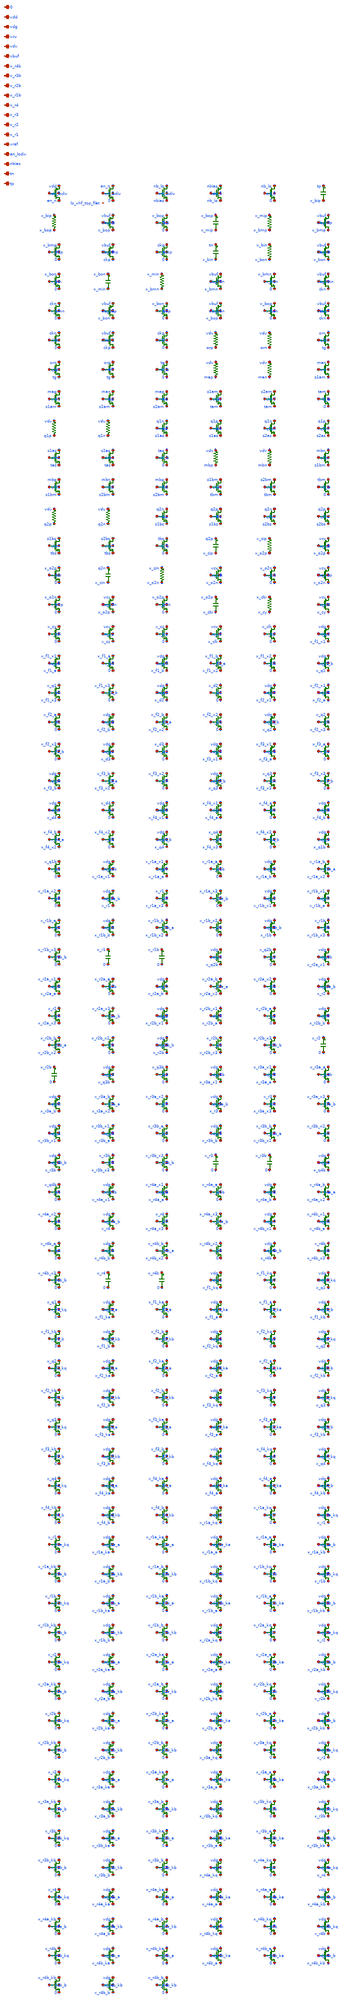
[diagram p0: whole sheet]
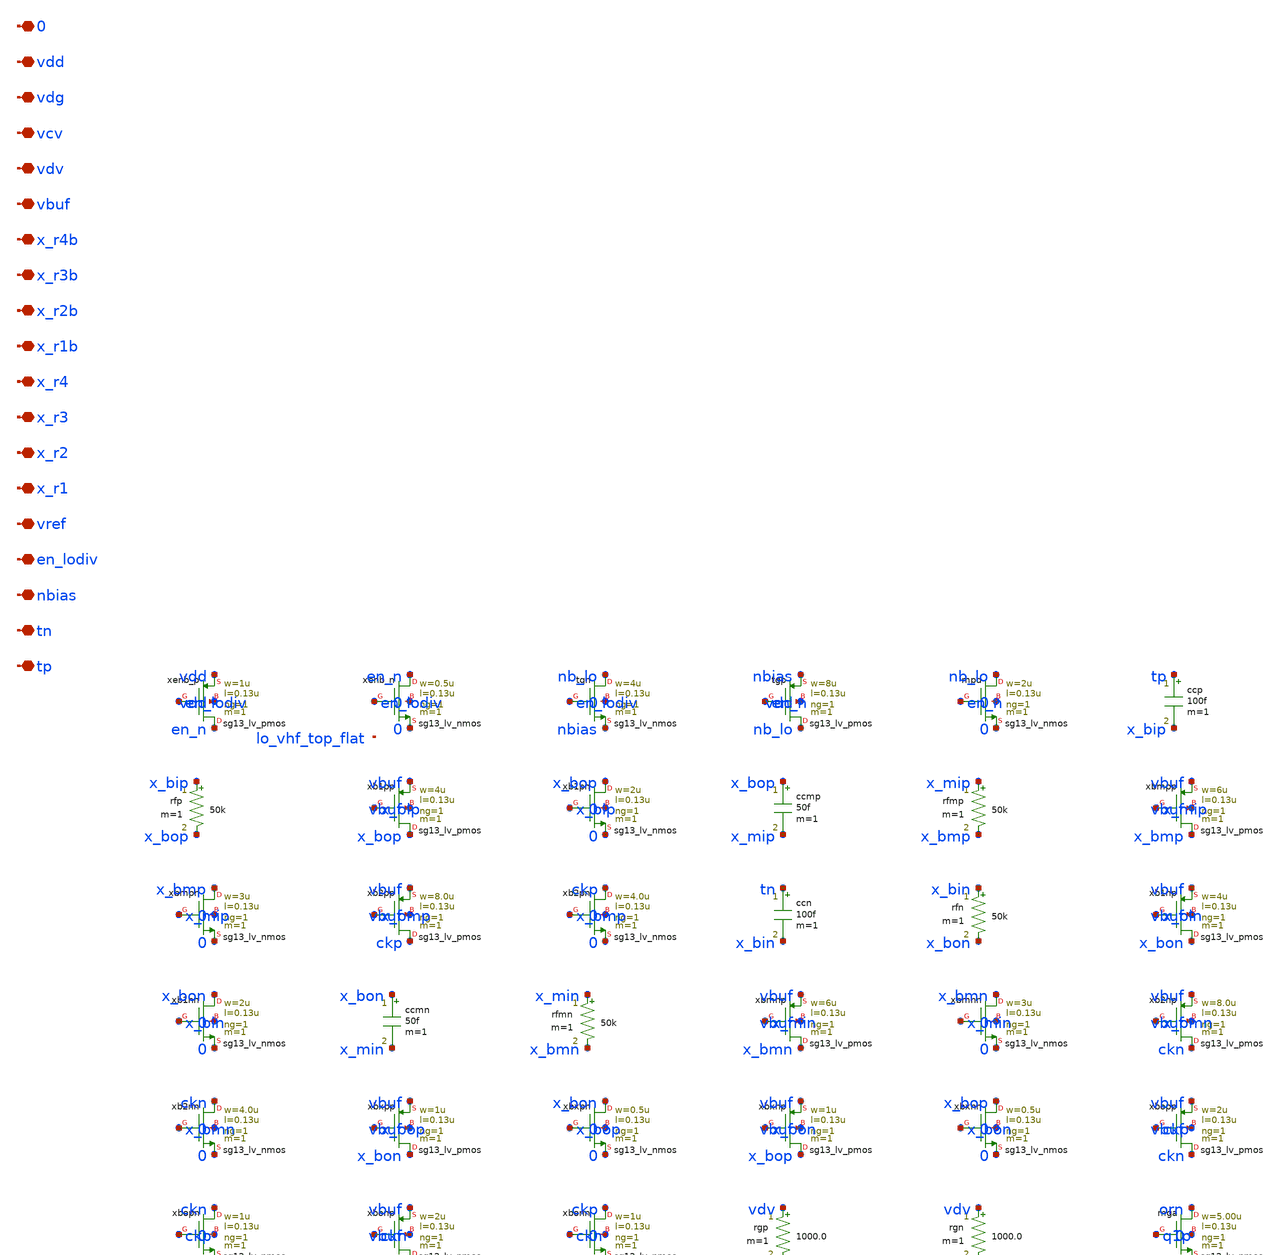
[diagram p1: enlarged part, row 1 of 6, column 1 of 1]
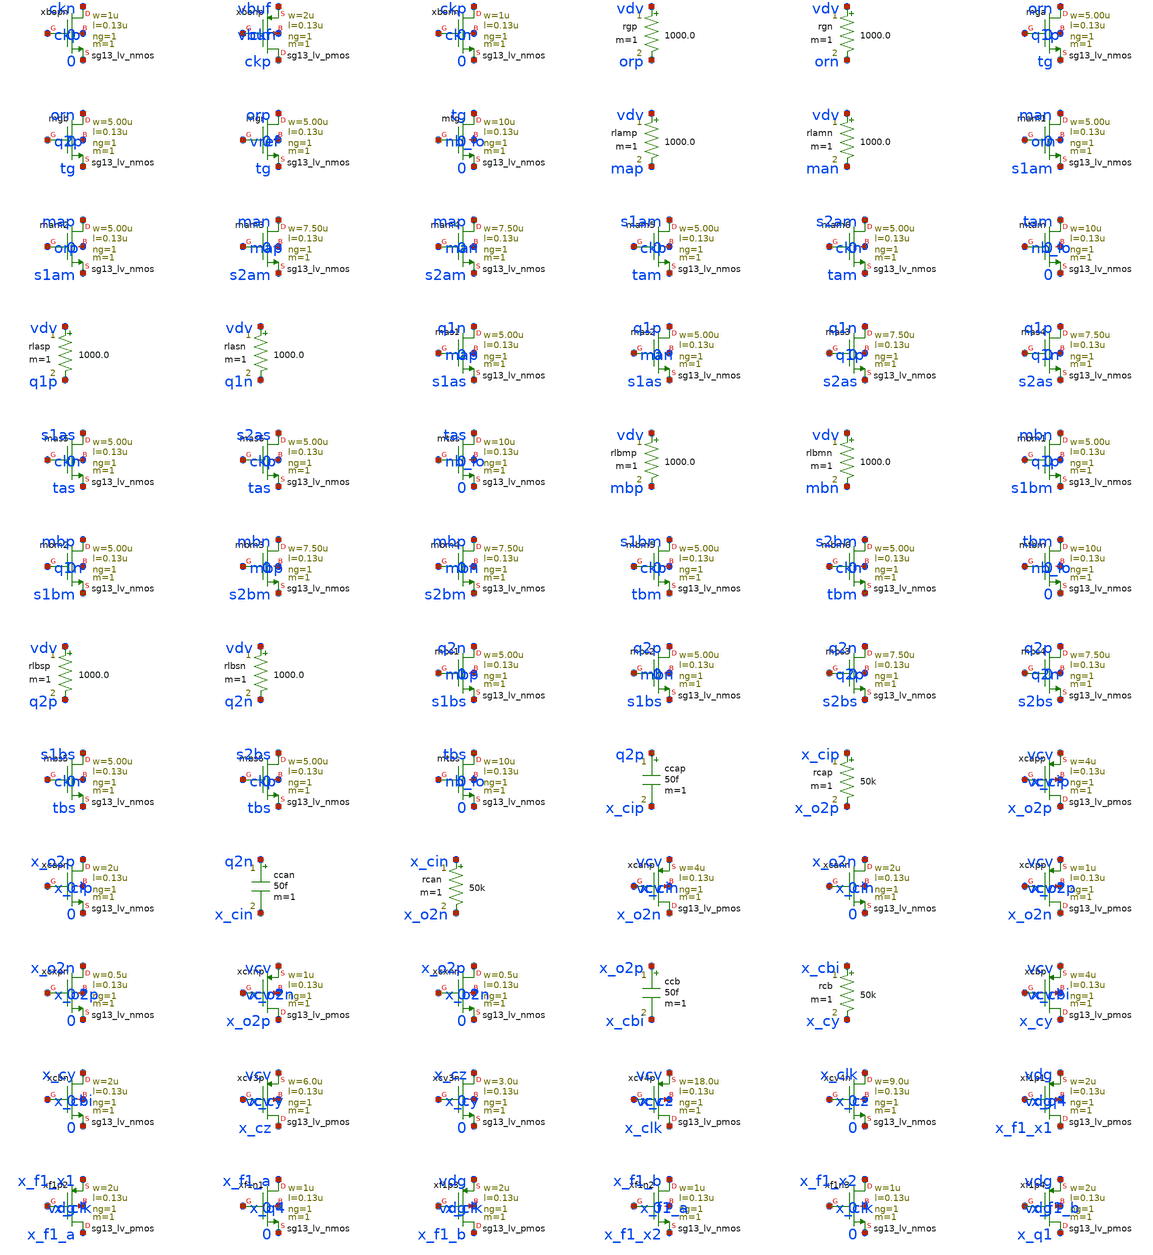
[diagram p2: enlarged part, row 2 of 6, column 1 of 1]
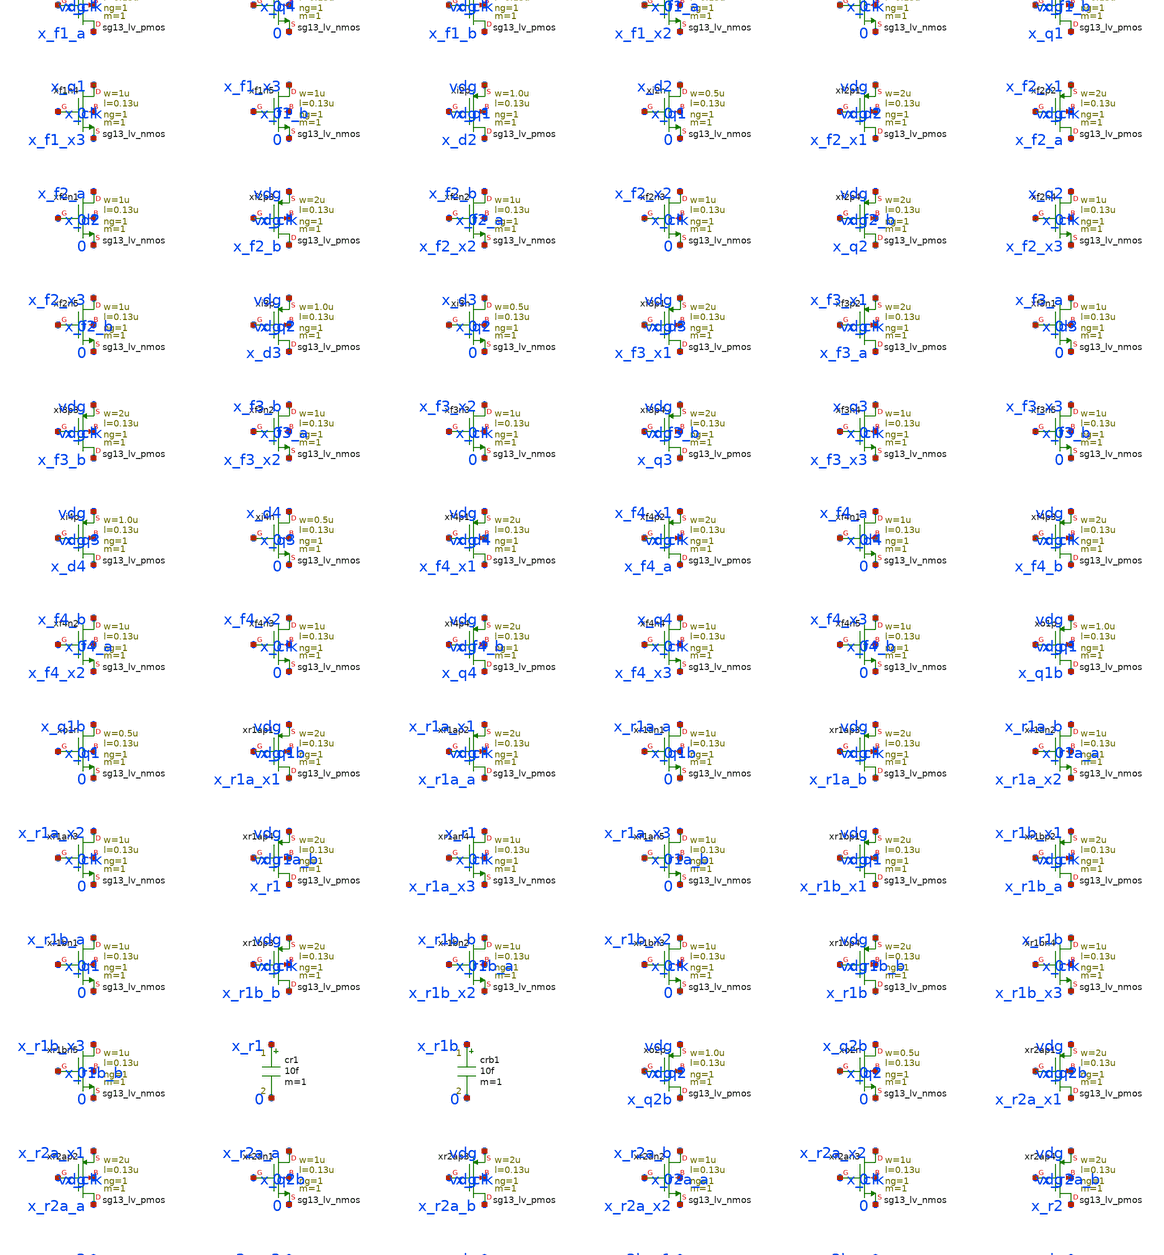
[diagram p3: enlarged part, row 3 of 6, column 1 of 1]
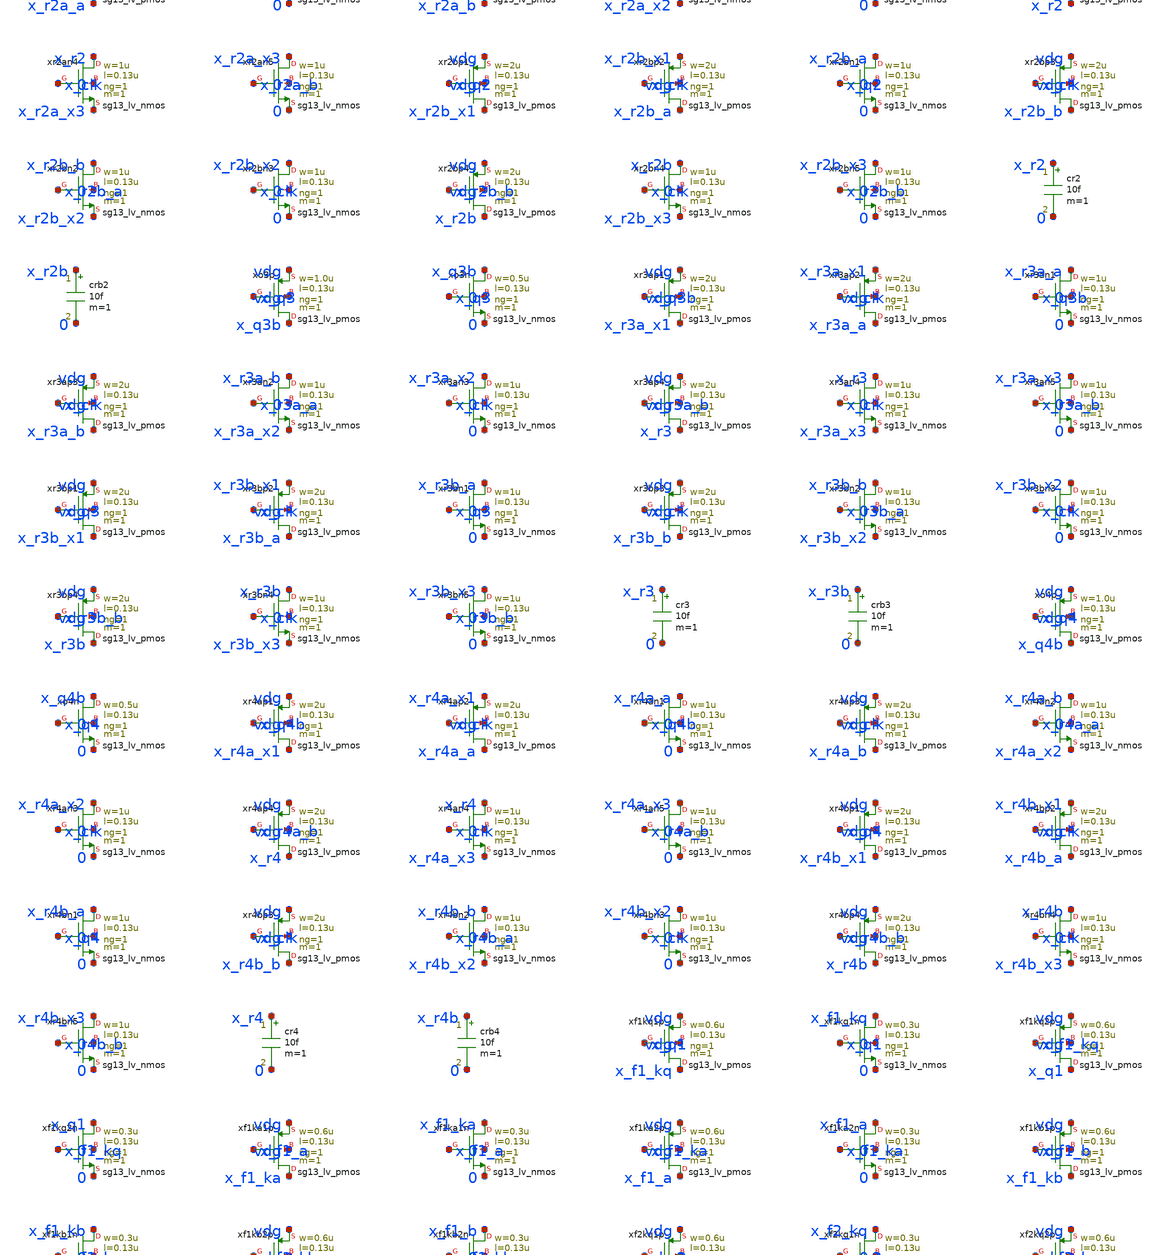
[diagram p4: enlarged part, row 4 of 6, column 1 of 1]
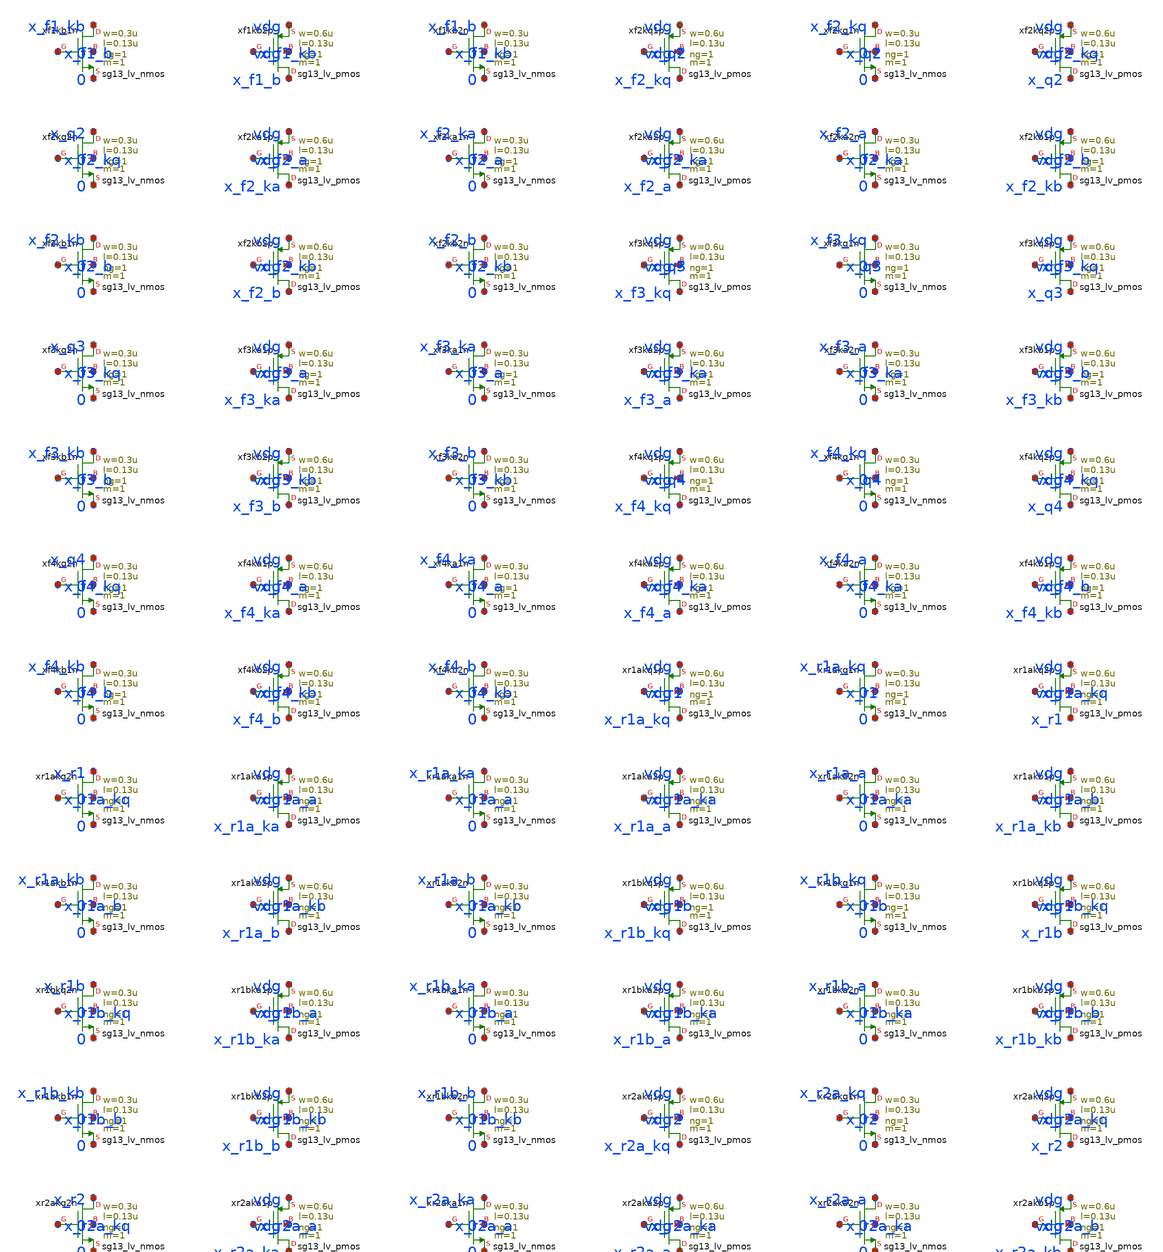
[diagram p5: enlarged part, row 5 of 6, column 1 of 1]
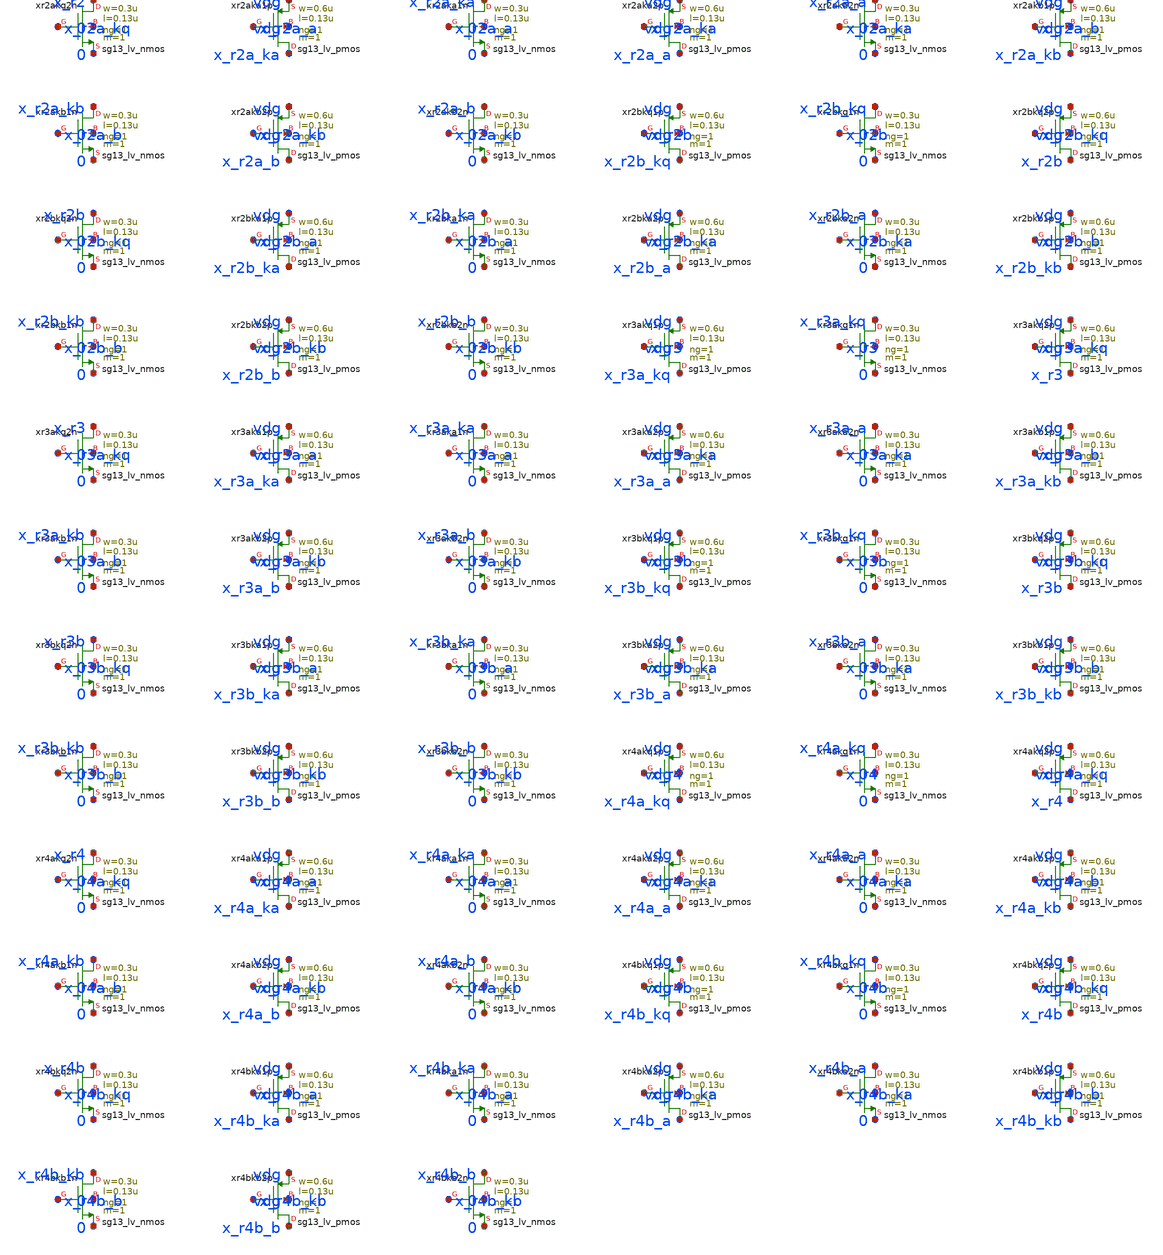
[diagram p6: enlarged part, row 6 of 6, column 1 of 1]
** sch_path: analog/lo/sch/lo_vhf_top.sch
**.subckt lo_vhf_top tp tn nbias en_lodiv vref x_r1 x_r2 x_r3 x_r4 x_r1b x_r2b x_r3b x_r4b vbuf vdv
*+ vcv vdg vdd 0
*.iopin tp
*.iopin tn
*.iopin nbias
*.iopin en_lodiv
*.iopin vref
*.iopin x_r1
*.iopin x_r2
*.iopin x_r3
*.iopin x_r4
*.iopin x_r1b
*.iopin x_r2b
*.iopin x_r3b
*.iopin x_r4b
*.iopin vbuf
*.iopin vdv
*.iopin vcv
*.iopin vdg
*.iopin vdd
*.iopin 0
Xxenb_p en_n en_lodiv vdd vdd sg13_lv_pmos w=1u l=0.13u ng=1 m=1 mm_ok=1
Xxenb_n en_n en_lodiv 0 0 sg13_lv_nmos w=0.5u l=0.13u ng=1 m=1 mm_ok=1
Xtgn nb_lo en_lodiv nbias 0 sg13_lv_nmos w=4u l=0.13u ng=1 m=1 mm_ok=1
Xtgp nb_lo en_n nbias vdd sg13_lv_pmos w=8u l=0.13u ng=1 m=1 mm_ok=1
Xmpd nb_lo en_n 0 0 sg13_lv_nmos w=2u l=0.13u ng=1 m=1 mm_ok=1
ccp tp x_bip 100f m=1
rfp x_bip x_bop 50k m=1
Xxb1pp x_bop x_bip vbuf vbuf sg13_lv_pmos w=4u l=0.13u ng=1 m=1 mm_ok=1
Xxb1pn x_bop x_bip 0 0 sg13_lv_nmos w=2u l=0.13u ng=1 m=1 mm_ok=1
ccmp x_bop x_mip 50f m=1
rfmp x_mip x_bmp 50k m=1
Xxbmpp x_bmp x_mip vbuf vbuf sg13_lv_pmos w=6u l=0.13u ng=1 m=1 mm_ok=1
Xxbmpn x_bmp x_mip 0 0 sg13_lv_nmos w=3u l=0.13u ng=1 m=1 mm_ok=1
Xxb2pp ckp x_bmp vbuf vbuf sg13_lv_pmos w=8.0u l=0.13u ng=1 m=1 mm_ok=1
Xxb2pn ckp x_bmp 0 0 sg13_lv_nmos w=4.0u l=0.13u ng=1 m=1 mm_ok=1
ccn tn x_bin 100f m=1
rfn x_bin x_bon 50k m=1
Xxb1np x_bon x_bin vbuf vbuf sg13_lv_pmos w=4u l=0.13u ng=1 m=1 mm_ok=1
Xxb1nn x_bon x_bin 0 0 sg13_lv_nmos w=2u l=0.13u ng=1 m=1 mm_ok=1
ccmn x_bon x_min 50f m=1
rfmn x_min x_bmn 50k m=1
Xxbmnp x_bmn x_min vbuf vbuf sg13_lv_pmos w=6u l=0.13u ng=1 m=1 mm_ok=1
Xxbmnn x_bmn x_min 0 0 sg13_lv_nmos w=3u l=0.13u ng=1 m=1 mm_ok=1
Xxb2np ckn x_bmn vbuf vbuf sg13_lv_pmos w=8.0u l=0.13u ng=1 m=1 mm_ok=1
Xxb2nn ckn x_bmn 0 0 sg13_lv_nmos w=4.0u l=0.13u ng=1 m=1 mm_ok=1
Xxbxpp x_bon x_bop vbuf vbuf sg13_lv_pmos w=1u l=0.13u ng=1 m=1 mm_ok=1
Xxbxpn x_bon x_bop 0 0 sg13_lv_nmos w=0.5u l=0.13u ng=1 m=1 mm_ok=1
Xxbxnp x_bop x_bon vbuf vbuf sg13_lv_pmos w=1u l=0.13u ng=1 m=1 mm_ok=1
Xxbxnn x_bop x_bon 0 0 sg13_lv_nmos w=0.5u l=0.13u ng=1 m=1 mm_ok=1
Xxbopp ckn ckp vbuf vbuf sg13_lv_pmos w=2u l=0.13u ng=1 m=1 mm_ok=1
Xxbopn ckn ckp 0 0 sg13_lv_nmos w=1u l=0.13u ng=1 m=1 mm_ok=1
Xxbonp ckp ckn vbuf vbuf sg13_lv_pmos w=2u l=0.13u ng=1 m=1 mm_ok=1
Xxbonn ckp ckn 0 0 sg13_lv_nmos w=1u l=0.13u ng=1 m=1 mm_ok=1
rgp vdv orp 1000.0 m=1
rgn vdv orn 1000.0 m=1
Xmga orn q1p tg 0 sg13_lv_nmos w=5.00u l=0.13u ng=1 m=1 mm_ok=1
Xmgb orn q2p tg 0 sg13_lv_nmos w=5.00u l=0.13u ng=1 m=1 mm_ok=1
Xmgr orp vref tg 0 sg13_lv_nmos w=5.00u l=0.13u ng=1 m=1 mm_ok=1
Xmtg tg nb_lo 0 0 sg13_lv_nmos w=10u l=0.13u ng=1 m=1 mm_ok=1
rlamp vdv map 1000.0 m=1
rlamn vdv man 1000.0 m=1
Xmam1 man orn s1am 0 sg13_lv_nmos w=5.00u l=0.13u ng=1 m=1 mm_ok=1
Xmam2 map orp s1am 0 sg13_lv_nmos w=5.00u l=0.13u ng=1 m=1 mm_ok=1
Xmam3 man map s2am 0 sg13_lv_nmos w=7.50u l=0.13u ng=1 m=1 mm_ok=1
Xmam4 map man s2am 0 sg13_lv_nmos w=7.50u l=0.13u ng=1 m=1 mm_ok=1
Xmam5 s1am ckp tam 0 sg13_lv_nmos w=5.00u l=0.13u ng=1 m=1 mm_ok=1
Xmam6 s2am ckn tam 0 sg13_lv_nmos w=5.00u l=0.13u ng=1 m=1 mm_ok=1
Xmtam tam nb_lo 0 0 sg13_lv_nmos w=10u l=0.13u ng=1 m=1 mm_ok=1
rlasp vdv q1p 1000.0 m=1
rlasn vdv q1n 1000.0 m=1
Xmas1 q1n map s1as 0 sg13_lv_nmos w=5.00u l=0.13u ng=1 m=1 mm_ok=1
Xmas2 q1p man s1as 0 sg13_lv_nmos w=5.00u l=0.13u ng=1 m=1 mm_ok=1
Xmas3 q1n q1p s2as 0 sg13_lv_nmos w=7.50u l=0.13u ng=1 m=1 mm_ok=1
Xmas4 q1p q1n s2as 0 sg13_lv_nmos w=7.50u l=0.13u ng=1 m=1 mm_ok=1
Xmas5 s1as ckn tas 0 sg13_lv_nmos w=5.00u l=0.13u ng=1 m=1 mm_ok=1
Xmas6 s2as ckp tas 0 sg13_lv_nmos w=5.00u l=0.13u ng=1 m=1 mm_ok=1
Xmtas tas nb_lo 0 0 sg13_lv_nmos w=10u l=0.13u ng=1 m=1 mm_ok=1
rlbmp vdv mbp 1000.0 m=1
rlbmn vdv mbn 1000.0 m=1
Xmbm1 mbn q1p s1bm 0 sg13_lv_nmos w=5.00u l=0.13u ng=1 m=1 mm_ok=1
Xmbm2 mbp q1n s1bm 0 sg13_lv_nmos w=5.00u l=0.13u ng=1 m=1 mm_ok=1
Xmbm3 mbn mbp s2bm 0 sg13_lv_nmos w=7.50u l=0.13u ng=1 m=1 mm_ok=1
Xmbm4 mbp mbn s2bm 0 sg13_lv_nmos w=7.50u l=0.13u ng=1 m=1 mm_ok=1
Xmbm5 s1bm ckp tbm 0 sg13_lv_nmos w=5.00u l=0.13u ng=1 m=1 mm_ok=1
Xmbm6 s2bm ckn tbm 0 sg13_lv_nmos w=5.00u l=0.13u ng=1 m=1 mm_ok=1
Xmtbm tbm nb_lo 0 0 sg13_lv_nmos w=10u l=0.13u ng=1 m=1 mm_ok=1
rlbsp vdv q2p 1000.0 m=1
rlbsn vdv q2n 1000.0 m=1
Xmbs1 q2n mbp s1bs 0 sg13_lv_nmos w=5.00u l=0.13u ng=1 m=1 mm_ok=1
Xmbs2 q2p mbn s1bs 0 sg13_lv_nmos w=5.00u l=0.13u ng=1 m=1 mm_ok=1
Xmbs3 q2n q2p s2bs 0 sg13_lv_nmos w=7.50u l=0.13u ng=1 m=1 mm_ok=1
Xmbs4 q2p q2n s2bs 0 sg13_lv_nmos w=7.50u l=0.13u ng=1 m=1 mm_ok=1
Xmbs5 s1bs ckn tbs 0 sg13_lv_nmos w=5.00u l=0.13u ng=1 m=1 mm_ok=1
Xmbs6 s2bs ckp tbs 0 sg13_lv_nmos w=5.00u l=0.13u ng=1 m=1 mm_ok=1
Xmtbs tbs nb_lo 0 0 sg13_lv_nmos w=10u l=0.13u ng=1 m=1 mm_ok=1
ccap q2p x_cip 50f m=1
rcap x_cip x_o2p 50k m=1
Xxcapp x_o2p x_cip vcv vcv sg13_lv_pmos w=4u l=0.13u ng=1 m=1 mm_ok=1
Xxcapn x_o2p x_cip 0 0 sg13_lv_nmos w=2u l=0.13u ng=1 m=1 mm_ok=1
ccan q2n x_cin 50f m=1
rcan x_cin x_o2n 50k m=1
Xxcanp x_o2n x_cin vcv vcv sg13_lv_pmos w=4u l=0.13u ng=1 m=1 mm_ok=1
Xxcann x_o2n x_cin 0 0 sg13_lv_nmos w=2u l=0.13u ng=1 m=1 mm_ok=1
Xxcxpp x_o2n x_o2p vcv vcv sg13_lv_pmos w=1u l=0.13u ng=1 m=1 mm_ok=1
Xxcxpn x_o2n x_o2p 0 0 sg13_lv_nmos w=0.5u l=0.13u ng=1 m=1 mm_ok=1
Xxcxnp x_o2p x_o2n vcv vcv sg13_lv_pmos w=1u l=0.13u ng=1 m=1 mm_ok=1
Xxcxnn x_o2p x_o2n 0 0 sg13_lv_nmos w=0.5u l=0.13u ng=1 m=1 mm_ok=1
ccb x_o2p x_cbi 50f m=1
rcb x_cbi x_cy 50k m=1
Xxcbp x_cy x_cbi vcv vcv sg13_lv_pmos w=4u l=0.13u ng=1 m=1 mm_ok=1
Xxcbn x_cy x_cbi 0 0 sg13_lv_nmos w=2u l=0.13u ng=1 m=1 mm_ok=1
Xxcv3p x_cz x_cy vcv vcv sg13_lv_pmos w=6.0u l=0.13u ng=1 m=1 mm_ok=1
Xxcv3n x_cz x_cy 0 0 sg13_lv_nmos w=3.0u l=0.13u ng=1 m=1 mm_ok=1
Xxcv4p x_clk x_cz vcv vcv sg13_lv_pmos w=18.0u l=0.13u ng=1 m=1 mm_ok=1
Xxcv4n x_clk x_cz 0 0 sg13_lv_nmos w=9.0u l=0.13u ng=1 m=1 mm_ok=1
Xxf1p1 x_f1_x1 x_q4 vdg vdg sg13_lv_pmos w=2u l=0.13u ng=1 m=1 mm_ok=1
Xxf1p2 x_f1_a x_clk x_f1_x1 vdg sg13_lv_pmos w=2u l=0.13u ng=1 m=1 mm_ok=1
Xxf1n1 x_f1_a x_q4 0 0 sg13_lv_nmos w=1u l=0.13u ng=1 m=1 mm_ok=1
Xxf1p3 x_f1_b x_clk vdg vdg sg13_lv_pmos w=2u l=0.13u ng=1 m=1 mm_ok=1
Xxf1n2 x_f1_b x_f1_a x_f1_x2 0 sg13_lv_nmos w=1u l=0.13u ng=1 m=1 mm_ok=1
Xxf1n3 x_f1_x2 x_clk 0 0 sg13_lv_nmos w=1u l=0.13u ng=1 m=1 mm_ok=1
Xxf1p4 x_q1 x_f1_b vdg vdg sg13_lv_pmos w=2u l=0.13u ng=1 m=1 mm_ok=1
Xxf1n4 x_q1 x_clk x_f1_x3 0 sg13_lv_nmos w=1u l=0.13u ng=1 m=1 mm_ok=1
Xxf1n5 x_f1_x3 x_f1_b 0 0 sg13_lv_nmos w=1u l=0.13u ng=1 m=1 mm_ok=1
Xxi2p x_d2 x_q1 vdg vdg sg13_lv_pmos w=1.0u l=0.13u ng=1 m=1 mm_ok=1
Xxi2n x_d2 x_q1 0 0 sg13_lv_nmos w=0.5u l=0.13u ng=1 m=1 mm_ok=1
Xxf2p1 x_f2_x1 x_d2 vdg vdg sg13_lv_pmos w=2u l=0.13u ng=1 m=1 mm_ok=1
Xxf2p2 x_f2_a x_clk x_f2_x1 vdg sg13_lv_pmos w=2u l=0.13u ng=1 m=1 mm_ok=1
Xxf2n1 x_f2_a x_d2 0 0 sg13_lv_nmos w=1u l=0.13u ng=1 m=1 mm_ok=1
Xxf2p3 x_f2_b x_clk vdg vdg sg13_lv_pmos w=2u l=0.13u ng=1 m=1 mm_ok=1
Xxf2n2 x_f2_b x_f2_a x_f2_x2 0 sg13_lv_nmos w=1u l=0.13u ng=1 m=1 mm_ok=1
Xxf2n3 x_f2_x2 x_clk 0 0 sg13_lv_nmos w=1u l=0.13u ng=1 m=1 mm_ok=1
Xxf2p4 x_q2 x_f2_b vdg vdg sg13_lv_pmos w=2u l=0.13u ng=1 m=1 mm_ok=1
Xxf2n4 x_q2 x_clk x_f2_x3 0 sg13_lv_nmos w=1u l=0.13u ng=1 m=1 mm_ok=1
Xxf2n5 x_f2_x3 x_f2_b 0 0 sg13_lv_nmos w=1u l=0.13u ng=1 m=1 mm_ok=1
Xxi3p x_d3 x_q2 vdg vdg sg13_lv_pmos w=1.0u l=0.13u ng=1 m=1 mm_ok=1
Xxi3n x_d3 x_q2 0 0 sg13_lv_nmos w=0.5u l=0.13u ng=1 m=1 mm_ok=1
Xxf3p1 x_f3_x1 x_d3 vdg vdg sg13_lv_pmos w=2u l=0.13u ng=1 m=1 mm_ok=1
Xxf3p2 x_f3_a x_clk x_f3_x1 vdg sg13_lv_pmos w=2u l=0.13u ng=1 m=1 mm_ok=1
Xxf3n1 x_f3_a x_d3 0 0 sg13_lv_nmos w=1u l=0.13u ng=1 m=1 mm_ok=1
Xxf3p3 x_f3_b x_clk vdg vdg sg13_lv_pmos w=2u l=0.13u ng=1 m=1 mm_ok=1
Xxf3n2 x_f3_b x_f3_a x_f3_x2 0 sg13_lv_nmos w=1u l=0.13u ng=1 m=1 mm_ok=1
Xxf3n3 x_f3_x2 x_clk 0 0 sg13_lv_nmos w=1u l=0.13u ng=1 m=1 mm_ok=1
Xxf3p4 x_q3 x_f3_b vdg vdg sg13_lv_pmos w=2u l=0.13u ng=1 m=1 mm_ok=1
Xxf3n4 x_q3 x_clk x_f3_x3 0 sg13_lv_nmos w=1u l=0.13u ng=1 m=1 mm_ok=1
Xxf3n5 x_f3_x3 x_f3_b 0 0 sg13_lv_nmos w=1u l=0.13u ng=1 m=1 mm_ok=1
Xxi4p x_d4 x_q3 vdg vdg sg13_lv_pmos w=1.0u l=0.13u ng=1 m=1 mm_ok=1
Xxi4n x_d4 x_q3 0 0 sg13_lv_nmos w=0.5u l=0.13u ng=1 m=1 mm_ok=1
Xxf4p1 x_f4_x1 x_d4 vdg vdg sg13_lv_pmos w=2u l=0.13u ng=1 m=1 mm_ok=1
Xxf4p2 x_f4_a x_clk x_f4_x1 vdg sg13_lv_pmos w=2u l=0.13u ng=1 m=1 mm_ok=1
Xxf4n1 x_f4_a x_d4 0 0 sg13_lv_nmos w=1u l=0.13u ng=1 m=1 mm_ok=1
Xxf4p3 x_f4_b x_clk vdg vdg sg13_lv_pmos w=2u l=0.13u ng=1 m=1 mm_ok=1
Xxf4n2 x_f4_b x_f4_a x_f4_x2 0 sg13_lv_nmos w=1u l=0.13u ng=1 m=1 mm_ok=1
Xxf4n3 x_f4_x2 x_clk 0 0 sg13_lv_nmos w=1u l=0.13u ng=1 m=1 mm_ok=1
Xxf4p4 x_q4 x_f4_b vdg vdg sg13_lv_pmos w=2u l=0.13u ng=1 m=1 mm_ok=1
Xxf4n4 x_q4 x_clk x_f4_x3 0 sg13_lv_nmos w=1u l=0.13u ng=1 m=1 mm_ok=1
Xxf4n5 x_f4_x3 x_f4_b 0 0 sg13_lv_nmos w=1u l=0.13u ng=1 m=1 mm_ok=1
Xxo1p x_q1b x_q1 vdg vdg sg13_lv_pmos w=1.0u l=0.13u ng=1 m=1 mm_ok=1
Xxo1n x_q1b x_q1 0 0 sg13_lv_nmos w=0.5u l=0.13u ng=1 m=1 mm_ok=1
Xxr1ap1 x_r1a_x1 x_q1b vdg vdg sg13_lv_pmos w=2u l=0.13u ng=1 m=1 mm_ok=1
Xxr1ap2 x_r1a_a x_clk x_r1a_x1 vdg sg13_lv_pmos w=2u l=0.13u ng=1 m=1 mm_ok=1
Xxr1an1 x_r1a_a x_q1b 0 0 sg13_lv_nmos w=1u l=0.13u ng=1 m=1 mm_ok=1
Xxr1ap3 x_r1a_b x_clk vdg vdg sg13_lv_pmos w=2u l=0.13u ng=1 m=1 mm_ok=1
Xxr1an2 x_r1a_b x_r1a_a x_r1a_x2 0 sg13_lv_nmos w=1u l=0.13u ng=1 m=1 mm_ok=1
Xxr1an3 x_r1a_x2 x_clk 0 0 sg13_lv_nmos w=1u l=0.13u ng=1 m=1 mm_ok=1
Xxr1ap4 x_r1 x_r1a_b vdg vdg sg13_lv_pmos w=2u l=0.13u ng=1 m=1 mm_ok=1
Xxr1an4 x_r1 x_clk x_r1a_x3 0 sg13_lv_nmos w=1u l=0.13u ng=1 m=1 mm_ok=1
Xxr1an5 x_r1a_x3 x_r1a_b 0 0 sg13_lv_nmos w=1u l=0.13u ng=1 m=1 mm_ok=1
Xxr1bp1 x_r1b_x1 x_q1 vdg vdg sg13_lv_pmos w=2u l=0.13u ng=1 m=1 mm_ok=1
Xxr1bp2 x_r1b_a x_clk x_r1b_x1 vdg sg13_lv_pmos w=2u l=0.13u ng=1 m=1 mm_ok=1
Xxr1bn1 x_r1b_a x_q1 0 0 sg13_lv_nmos w=1u l=0.13u ng=1 m=1 mm_ok=1
Xxr1bp3 x_r1b_b x_clk vdg vdg sg13_lv_pmos w=2u l=0.13u ng=1 m=1 mm_ok=1
Xxr1bn2 x_r1b_b x_r1b_a x_r1b_x2 0 sg13_lv_nmos w=1u l=0.13u ng=1 m=1 mm_ok=1
Xxr1bn3 x_r1b_x2 x_clk 0 0 sg13_lv_nmos w=1u l=0.13u ng=1 m=1 mm_ok=1
Xxr1bp4 x_r1b x_r1b_b vdg vdg sg13_lv_pmos w=2u l=0.13u ng=1 m=1 mm_ok=1
Xxr1bn4 x_r1b x_clk x_r1b_x3 0 sg13_lv_nmos w=1u l=0.13u ng=1 m=1 mm_ok=1
Xxr1bn5 x_r1b_x3 x_r1b_b 0 0 sg13_lv_nmos w=1u l=0.13u ng=1 m=1 mm_ok=1
cr1 x_r1 0 10f m=1
crb1 x_r1b 0 10f m=1
Xxo2p x_q2b x_q2 vdg vdg sg13_lv_pmos w=1.0u l=0.13u ng=1 m=1 mm_ok=1
Xxo2n x_q2b x_q2 0 0 sg13_lv_nmos w=0.5u l=0.13u ng=1 m=1 mm_ok=1
Xxr2ap1 x_r2a_x1 x_q2b vdg vdg sg13_lv_pmos w=2u l=0.13u ng=1 m=1 mm_ok=1
Xxr2ap2 x_r2a_a x_clk x_r2a_x1 vdg sg13_lv_pmos w=2u l=0.13u ng=1 m=1 mm_ok=1
Xxr2an1 x_r2a_a x_q2b 0 0 sg13_lv_nmos w=1u l=0.13u ng=1 m=1 mm_ok=1
Xxr2ap3 x_r2a_b x_clk vdg vdg sg13_lv_pmos w=2u l=0.13u ng=1 m=1 mm_ok=1
Xxr2an2 x_r2a_b x_r2a_a x_r2a_x2 0 sg13_lv_nmos w=1u l=0.13u ng=1 m=1 mm_ok=1
Xxr2an3 x_r2a_x2 x_clk 0 0 sg13_lv_nmos w=1u l=0.13u ng=1 m=1 mm_ok=1
Xxr2ap4 x_r2 x_r2a_b vdg vdg sg13_lv_pmos w=2u l=0.13u ng=1 m=1 mm_ok=1
Xxr2an4 x_r2 x_clk x_r2a_x3 0 sg13_lv_nmos w=1u l=0.13u ng=1 m=1 mm_ok=1
Xxr2an5 x_r2a_x3 x_r2a_b 0 0 sg13_lv_nmos w=1u l=0.13u ng=1 m=1 mm_ok=1
Xxr2bp1 x_r2b_x1 x_q2 vdg vdg sg13_lv_pmos w=2u l=0.13u ng=1 m=1 mm_ok=1
Xxr2bp2 x_r2b_a x_clk x_r2b_x1 vdg sg13_lv_pmos w=2u l=0.13u ng=1 m=1 mm_ok=1
Xxr2bn1 x_r2b_a x_q2 0 0 sg13_lv_nmos w=1u l=0.13u ng=1 m=1 mm_ok=1
Xxr2bp3 x_r2b_b x_clk vdg vdg sg13_lv_pmos w=2u l=0.13u ng=1 m=1 mm_ok=1
Xxr2bn2 x_r2b_b x_r2b_a x_r2b_x2 0 sg13_lv_nmos w=1u l=0.13u ng=1 m=1 mm_ok=1
Xxr2bn3 x_r2b_x2 x_clk 0 0 sg13_lv_nmos w=1u l=0.13u ng=1 m=1 mm_ok=1
Xxr2bp4 x_r2b x_r2b_b vdg vdg sg13_lv_pmos w=2u l=0.13u ng=1 m=1 mm_ok=1
Xxr2bn4 x_r2b x_clk x_r2b_x3 0 sg13_lv_nmos w=1u l=0.13u ng=1 m=1 mm_ok=1
Xxr2bn5 x_r2b_x3 x_r2b_b 0 0 sg13_lv_nmos w=1u l=0.13u ng=1 m=1 mm_ok=1
cr2 x_r2 0 10f m=1
crb2 x_r2b 0 10f m=1
Xxo3p x_q3b x_q3 vdg vdg sg13_lv_pmos w=1.0u l=0.13u ng=1 m=1 mm_ok=1
Xxo3n x_q3b x_q3 0 0 sg13_lv_nmos w=0.5u l=0.13u ng=1 m=1 mm_ok=1
Xxr3ap1 x_r3a_x1 x_q3b vdg vdg sg13_lv_pmos w=2u l=0.13u ng=1 m=1 mm_ok=1
Xxr3ap2 x_r3a_a x_clk x_r3a_x1 vdg sg13_lv_pmos w=2u l=0.13u ng=1 m=1 mm_ok=1
Xxr3an1 x_r3a_a x_q3b 0 0 sg13_lv_nmos w=1u l=0.13u ng=1 m=1 mm_ok=1
Xxr3ap3 x_r3a_b x_clk vdg vdg sg13_lv_pmos w=2u l=0.13u ng=1 m=1 mm_ok=1
Xxr3an2 x_r3a_b x_r3a_a x_r3a_x2 0 sg13_lv_nmos w=1u l=0.13u ng=1 m=1 mm_ok=1
Xxr3an3 x_r3a_x2 x_clk 0 0 sg13_lv_nmos w=1u l=0.13u ng=1 m=1 mm_ok=1
Xxr3ap4 x_r3 x_r3a_b vdg vdg sg13_lv_pmos w=2u l=0.13u ng=1 m=1 mm_ok=1
Xxr3an4 x_r3 x_clk x_r3a_x3 0 sg13_lv_nmos w=1u l=0.13u ng=1 m=1 mm_ok=1
Xxr3an5 x_r3a_x3 x_r3a_b 0 0 sg13_lv_nmos w=1u l=0.13u ng=1 m=1 mm_ok=1
Xxr3bp1 x_r3b_x1 x_q3 vdg vdg sg13_lv_pmos w=2u l=0.13u ng=1 m=1 mm_ok=1
Xxr3bp2 x_r3b_a x_clk x_r3b_x1 vdg sg13_lv_pmos w=2u l=0.13u ng=1 m=1 mm_ok=1
Xxr3bn1 x_r3b_a x_q3 0 0 sg13_lv_nmos w=1u l=0.13u ng=1 m=1 mm_ok=1
Xxr3bp3 x_r3b_b x_clk vdg vdg sg13_lv_pmos w=2u l=0.13u ng=1 m=1 mm_ok=1
Xxr3bn2 x_r3b_b x_r3b_a x_r3b_x2 0 sg13_lv_nmos w=1u l=0.13u ng=1 m=1 mm_ok=1
Xxr3bn3 x_r3b_x2 x_clk 0 0 sg13_lv_nmos w=1u l=0.13u ng=1 m=1 mm_ok=1
Xxr3bp4 x_r3b x_r3b_b vdg vdg sg13_lv_pmos w=2u l=0.13u ng=1 m=1 mm_ok=1
Xxr3bn4 x_r3b x_clk x_r3b_x3 0 sg13_lv_nmos w=1u l=0.13u ng=1 m=1 mm_ok=1
Xxr3bn5 x_r3b_x3 x_r3b_b 0 0 sg13_lv_nmos w=1u l=0.13u ng=1 m=1 mm_ok=1
cr3 x_r3 0 10f m=1
crb3 x_r3b 0 10f m=1
Xxo4p x_q4b x_q4 vdg vdg sg13_lv_pmos w=1.0u l=0.13u ng=1 m=1 mm_ok=1
Xxo4n x_q4b x_q4 0 0 sg13_lv_nmos w=0.5u l=0.13u ng=1 m=1 mm_ok=1
Xxr4ap1 x_r4a_x1 x_q4b vdg vdg sg13_lv_pmos w=2u l=0.13u ng=1 m=1 mm_ok=1
Xxr4ap2 x_r4a_a x_clk x_r4a_x1 vdg sg13_lv_pmos w=2u l=0.13u ng=1 m=1 mm_ok=1
Xxr4an1 x_r4a_a x_q4b 0 0 sg13_lv_nmos w=1u l=0.13u ng=1 m=1 mm_ok=1
Xxr4ap3 x_r4a_b x_clk vdg vdg sg13_lv_pmos w=2u l=0.13u ng=1 m=1 mm_ok=1
Xxr4an2 x_r4a_b x_r4a_a x_r4a_x2 0 sg13_lv_nmos w=1u l=0.13u ng=1 m=1 mm_ok=1
Xxr4an3 x_r4a_x2 x_clk 0 0 sg13_lv_nmos w=1u l=0.13u ng=1 m=1 mm_ok=1
Xxr4ap4 x_r4 x_r4a_b vdg vdg sg13_lv_pmos w=2u l=0.13u ng=1 m=1 mm_ok=1
Xxr4an4 x_r4 x_clk x_r4a_x3 0 sg13_lv_nmos w=1u l=0.13u ng=1 m=1 mm_ok=1
Xxr4an5 x_r4a_x3 x_r4a_b 0 0 sg13_lv_nmos w=1u l=0.13u ng=1 m=1 mm_ok=1
Xxr4bp1 x_r4b_x1 x_q4 vdg vdg sg13_lv_pmos w=2u l=0.13u ng=1 m=1 mm_ok=1
Xxr4bp2 x_r4b_a x_clk x_r4b_x1 vdg sg13_lv_pmos w=2u l=0.13u ng=1 m=1 mm_ok=1
Xxr4bn1 x_r4b_a x_q4 0 0 sg13_lv_nmos w=1u l=0.13u ng=1 m=1 mm_ok=1
Xxr4bp3 x_r4b_b x_clk vdg vdg sg13_lv_pmos w=2u l=0.13u ng=1 m=1 mm_ok=1
Xxr4bn2 x_r4b_b x_r4b_a x_r4b_x2 0 sg13_lv_nmos w=1u l=0.13u ng=1 m=1 mm_ok=1
Xxr4bn3 x_r4b_x2 x_clk 0 0 sg13_lv_nmos w=1u l=0.13u ng=1 m=1 mm_ok=1
Xxr4bp4 x_r4b x_r4b_b vdg vdg sg13_lv_pmos w=2u l=0.13u ng=1 m=1 mm_ok=1
Xxr4bn4 x_r4b x_clk x_r4b_x3 0 sg13_lv_nmos w=1u l=0.13u ng=1 m=1 mm_ok=1
Xxr4bn5 x_r4b_x3 x_r4b_b 0 0 sg13_lv_nmos w=1u l=0.13u ng=1 m=1 mm_ok=1
cr4 x_r4 0 10f m=1
crb4 x_r4b 0 10f m=1
Xxf1kq1p x_f1_kq x_q1 vdg vdg sg13_lv_pmos w=0.6u l=0.13u ng=1 m=1 mm_ok=1
Xxf1kq1n x_f1_kq x_q1 0 0 sg13_lv_nmos w=0.3u l=0.13u ng=1 m=1 mm_ok=1
Xxf1kq2p x_q1 x_f1_kq vdg vdg sg13_lv_pmos w=0.6u l=0.13u ng=1 m=1 mm_ok=1
Xxf1kq2n x_q1 x_f1_kq 0 0 sg13_lv_nmos w=0.3u l=0.13u ng=1 m=1 mm_ok=1
Xxf1ka1p x_f1_ka x_f1_a vdg vdg sg13_lv_pmos w=0.6u l=0.13u ng=1 m=1 mm_ok=1
Xxf1ka1n x_f1_ka x_f1_a 0 0 sg13_lv_nmos w=0.3u l=0.13u ng=1 m=1 mm_ok=1
Xxf1ka2p x_f1_a x_f1_ka vdg vdg sg13_lv_pmos w=0.6u l=0.13u ng=1 m=1 mm_ok=1
Xxf1ka2n x_f1_a x_f1_ka 0 0 sg13_lv_nmos w=0.3u l=0.13u ng=1 m=1 mm_ok=1
Xxf1kb1p x_f1_kb x_f1_b vdg vdg sg13_lv_pmos w=0.6u l=0.13u ng=1 m=1 mm_ok=1
Xxf1kb1n x_f1_kb x_f1_b 0 0 sg13_lv_nmos w=0.3u l=0.13u ng=1 m=1 mm_ok=1
Xxf1kb2p x_f1_b x_f1_kb vdg vdg sg13_lv_pmos w=0.6u l=0.13u ng=1 m=1 mm_ok=1
Xxf1kb2n x_f1_b x_f1_kb 0 0 sg13_lv_nmos w=0.3u l=0.13u ng=1 m=1 mm_ok=1
Xxf2kq1p x_f2_kq x_q2 vdg vdg sg13_lv_pmos w=0.6u l=0.13u ng=1 m=1 mm_ok=1
Xxf2kq1n x_f2_kq x_q2 0 0 sg13_lv_nmos w=0.3u l=0.13u ng=1 m=1 mm_ok=1
Xxf2kq2p x_q2 x_f2_kq vdg vdg sg13_lv_pmos w=0.6u l=0.13u ng=1 m=1 mm_ok=1
Xxf2kq2n x_q2 x_f2_kq 0 0 sg13_lv_nmos w=0.3u l=0.13u ng=1 m=1 mm_ok=1
Xxf2ka1p x_f2_ka x_f2_a vdg vdg sg13_lv_pmos w=0.6u l=0.13u ng=1 m=1 mm_ok=1
Xxf2ka1n x_f2_ka x_f2_a 0 0 sg13_lv_nmos w=0.3u l=0.13u ng=1 m=1 mm_ok=1
Xxf2ka2p x_f2_a x_f2_ka vdg vdg sg13_lv_pmos w=0.6u l=0.13u ng=1 m=1 mm_ok=1
Xxf2ka2n x_f2_a x_f2_ka 0 0 sg13_lv_nmos w=0.3u l=0.13u ng=1 m=1 mm_ok=1
Xxf2kb1p x_f2_kb x_f2_b vdg vdg sg13_lv_pmos w=0.6u l=0.13u ng=1 m=1 mm_ok=1
Xxf2kb1n x_f2_kb x_f2_b 0 0 sg13_lv_nmos w=0.3u l=0.13u ng=1 m=1 mm_ok=1
Xxf2kb2p x_f2_b x_f2_kb vdg vdg sg13_lv_pmos w=0.6u l=0.13u ng=1 m=1 mm_ok=1
Xxf2kb2n x_f2_b x_f2_kb 0 0 sg13_lv_nmos w=0.3u l=0.13u ng=1 m=1 mm_ok=1
Xxf3kq1p x_f3_kq x_q3 vdg vdg sg13_lv_pmos w=0.6u l=0.13u ng=1 m=1 mm_ok=1
Xxf3kq1n x_f3_kq x_q3 0 0 sg13_lv_nmos w=0.3u l=0.13u ng=1 m=1 mm_ok=1
Xxf3kq2p x_q3 x_f3_kq vdg vdg sg13_lv_pmos w=0.6u l=0.13u ng=1 m=1 mm_ok=1
Xxf3kq2n x_q3 x_f3_kq 0 0 sg13_lv_nmos w=0.3u l=0.13u ng=1 m=1 mm_ok=1
Xxf3ka1p x_f3_ka x_f3_a vdg vdg sg13_lv_pmos w=0.6u l=0.13u ng=1 m=1 mm_ok=1
Xxf3ka1n x_f3_ka x_f3_a 0 0 sg13_lv_nmos w=0.3u l=0.13u ng=1 m=1 mm_ok=1
Xxf3ka2p x_f3_a x_f3_ka vdg vdg sg13_lv_pmos w=0.6u l=0.13u ng=1 m=1 mm_ok=1
Xxf3ka2n x_f3_a x_f3_ka 0 0 sg13_lv_nmos w=0.3u l=0.13u ng=1 m=1 mm_ok=1
Xxf3kb1p x_f3_kb x_f3_b vdg vdg sg13_lv_pmos w=0.6u l=0.13u ng=1 m=1 mm_ok=1
Xxf3kb1n x_f3_kb x_f3_b 0 0 sg13_lv_nmos w=0.3u l=0.13u ng=1 m=1 mm_ok=1
Xxf3kb2p x_f3_b x_f3_kb vdg vdg sg13_lv_pmos w=0.6u l=0.13u ng=1 m=1 mm_ok=1
Xxf3kb2n x_f3_b x_f3_kb 0 0 sg13_lv_nmos w=0.3u l=0.13u ng=1 m=1 mm_ok=1
Xxf4kq1p x_f4_kq x_q4 vdg vdg sg13_lv_pmos w=0.6u l=0.13u ng=1 m=1 mm_ok=1
Xxf4kq1n x_f4_kq x_q4 0 0 sg13_lv_nmos w=0.3u l=0.13u ng=1 m=1 mm_ok=1
Xxf4kq2p x_q4 x_f4_kq vdg vdg sg13_lv_pmos w=0.6u l=0.13u ng=1 m=1 mm_ok=1
Xxf4kq2n x_q4 x_f4_kq 0 0 sg13_lv_nmos w=0.3u l=0.13u ng=1 m=1 mm_ok=1
Xxf4ka1p x_f4_ka x_f4_a vdg vdg sg13_lv_pmos w=0.6u l=0.13u ng=1 m=1 mm_ok=1
Xxf4ka1n x_f4_ka x_f4_a 0 0 sg13_lv_nmos w=0.3u l=0.13u ng=1 m=1 mm_ok=1
Xxf4ka2p x_f4_a x_f4_ka vdg vdg sg13_lv_pmos w=0.6u l=0.13u ng=1 m=1 mm_ok=1
Xxf4ka2n x_f4_a x_f4_ka 0 0 sg13_lv_nmos w=0.3u l=0.13u ng=1 m=1 mm_ok=1
Xxf4kb1p x_f4_kb x_f4_b vdg vdg sg13_lv_pmos w=0.6u l=0.13u ng=1 m=1 mm_ok=1
Xxf4kb1n x_f4_kb x_f4_b 0 0 sg13_lv_nmos w=0.3u l=0.13u ng=1 m=1 mm_ok=1
Xxf4kb2p x_f4_b x_f4_kb vdg vdg sg13_lv_pmos w=0.6u l=0.13u ng=1 m=1 mm_ok=1
Xxf4kb2n x_f4_b x_f4_kb 0 0 sg13_lv_nmos w=0.3u l=0.13u ng=1 m=1 mm_ok=1
Xxr1akq1p x_r1a_kq x_r1 vdg vdg sg13_lv_pmos w=0.6u l=0.13u ng=1 m=1 mm_ok=1
Xxr1akq1n x_r1a_kq x_r1 0 0 sg13_lv_nmos w=0.3u l=0.13u ng=1 m=1 mm_ok=1
Xxr1akq2p x_r1 x_r1a_kq vdg vdg sg13_lv_pmos w=0.6u l=0.13u ng=1 m=1 mm_ok=1
Xxr1akq2n x_r1 x_r1a_kq 0 0 sg13_lv_nmos w=0.3u l=0.13u ng=1 m=1 mm_ok=1
Xxr1aka1p x_r1a_ka x_r1a_a vdg vdg sg13_lv_pmos w=0.6u l=0.13u ng=1 m=1 mm_ok=1
Xxr1aka1n x_r1a_ka x_r1a_a 0 0 sg13_lv_nmos w=0.3u l=0.13u ng=1 m=1 mm_ok=1
Xxr1aka2p x_r1a_a x_r1a_ka vdg vdg sg13_lv_pmos w=0.6u l=0.13u ng=1 m=1 mm_ok=1
Xxr1aka2n x_r1a_a x_r1a_ka 0 0 sg13_lv_nmos w=0.3u l=0.13u ng=1 m=1 mm_ok=1
Xxr1akb1p x_r1a_kb x_r1a_b vdg vdg sg13_lv_pmos w=0.6u l=0.13u ng=1 m=1 mm_ok=1
Xxr1akb1n x_r1a_kb x_r1a_b 0 0 sg13_lv_nmos w=0.3u l=0.13u ng=1 m=1 mm_ok=1
Xxr1akb2p x_r1a_b x_r1a_kb vdg vdg sg13_lv_pmos w=0.6u l=0.13u ng=1 m=1 mm_ok=1
Xxr1akb2n x_r1a_b x_r1a_kb 0 0 sg13_lv_nmos w=0.3u l=0.13u ng=1 m=1 mm_ok=1
Xxr1bkq1p x_r1b_kq x_r1b vdg vdg sg13_lv_pmos w=0.6u l=0.13u ng=1 m=1 mm_ok=1
Xxr1bkq1n x_r1b_kq x_r1b 0 0 sg13_lv_nmos w=0.3u l=0.13u ng=1 m=1 mm_ok=1
Xxr1bkq2p x_r1b x_r1b_kq vdg vdg sg13_lv_pmos w=0.6u l=0.13u ng=1 m=1 mm_ok=1
Xxr1bkq2n x_r1b x_r1b_kq 0 0 sg13_lv_nmos w=0.3u l=0.13u ng=1 m=1 mm_ok=1
Xxr1bka1p x_r1b_ka x_r1b_a vdg vdg sg13_lv_pmos w=0.6u l=0.13u ng=1 m=1 mm_ok=1
Xxr1bka1n x_r1b_ka x_r1b_a 0 0 sg13_lv_nmos w=0.3u l=0.13u ng=1 m=1 mm_ok=1
Xxr1bka2p x_r1b_a x_r1b_ka vdg vdg sg13_lv_pmos w=0.6u l=0.13u ng=1 m=1 mm_ok=1
Xxr1bka2n x_r1b_a x_r1b_ka 0 0 sg13_lv_nmos w=0.3u l=0.13u ng=1 m=1 mm_ok=1
Xxr1bkb1p x_r1b_kb x_r1b_b vdg vdg sg13_lv_pmos w=0.6u l=0.13u ng=1 m=1 mm_ok=1
Xxr1bkb1n x_r1b_kb x_r1b_b 0 0 sg13_lv_nmos w=0.3u l=0.13u ng=1 m=1 mm_ok=1
Xxr1bkb2p x_r1b_b x_r1b_kb vdg vdg sg13_lv_pmos w=0.6u l=0.13u ng=1 m=1 mm_ok=1
Xxr1bkb2n x_r1b_b x_r1b_kb 0 0 sg13_lv_nmos w=0.3u l=0.13u ng=1 m=1 mm_ok=1
Xxr2akq1p x_r2a_kq x_r2 vdg vdg sg13_lv_pmos w=0.6u l=0.13u ng=1 m=1 mm_ok=1
Xxr2akq1n x_r2a_kq x_r2 0 0 sg13_lv_nmos w=0.3u l=0.13u ng=1 m=1 mm_ok=1
Xxr2akq2p x_r2 x_r2a_kq vdg vdg sg13_lv_pmos w=0.6u l=0.13u ng=1 m=1 mm_ok=1
Xxr2akq2n x_r2 x_r2a_kq 0 0 sg13_lv_nmos w=0.3u l=0.13u ng=1 m=1 mm_ok=1
Xxr2aka1p x_r2a_ka x_r2a_a vdg vdg sg13_lv_pmos w=0.6u l=0.13u ng=1 m=1 mm_ok=1
Xxr2aka1n x_r2a_ka x_r2a_a 0 0 sg13_lv_nmos w=0.3u l=0.13u ng=1 m=1 mm_ok=1
Xxr2aka2p x_r2a_a x_r2a_ka vdg vdg sg13_lv_pmos w=0.6u l=0.13u ng=1 m=1 mm_ok=1
Xxr2aka2n x_r2a_a x_r2a_ka 0 0 sg13_lv_nmos w=0.3u l=0.13u ng=1 m=1 mm_ok=1
Xxr2akb1p x_r2a_kb x_r2a_b vdg vdg sg13_lv_pmos w=0.6u l=0.13u ng=1 m=1 mm_ok=1
Xxr2akb1n x_r2a_kb x_r2a_b 0 0 sg13_lv_nmos w=0.3u l=0.13u ng=1 m=1 mm_ok=1
Xxr2akb2p x_r2a_b x_r2a_kb vdg vdg sg13_lv_pmos w=0.6u l=0.13u ng=1 m=1 mm_ok=1
Xxr2akb2n x_r2a_b x_r2a_kb 0 0 sg13_lv_nmos w=0.3u l=0.13u ng=1 m=1 mm_ok=1
Xxr2bkq1p x_r2b_kq x_r2b vdg vdg sg13_lv_pmos w=0.6u l=0.13u ng=1 m=1 mm_ok=1
Xxr2bkq1n x_r2b_kq x_r2b 0 0 sg13_lv_nmos w=0.3u l=0.13u ng=1 m=1 mm_ok=1
Xxr2bkq2p x_r2b x_r2b_kq vdg vdg sg13_lv_pmos w=0.6u l=0.13u ng=1 m=1 mm_ok=1
Xxr2bkq2n x_r2b x_r2b_kq 0 0 sg13_lv_nmos w=0.3u l=0.13u ng=1 m=1 mm_ok=1
Xxr2bka1p x_r2b_ka x_r2b_a vdg vdg sg13_lv_pmos w=0.6u l=0.13u ng=1 m=1 mm_ok=1
Xxr2bka1n x_r2b_ka x_r2b_a 0 0 sg13_lv_nmos w=0.3u l=0.13u ng=1 m=1 mm_ok=1
Xxr2bka2p x_r2b_a x_r2b_ka vdg vdg sg13_lv_pmos w=0.6u l=0.13u ng=1 m=1 mm_ok=1
Xxr2bka2n x_r2b_a x_r2b_ka 0 0 sg13_lv_nmos w=0.3u l=0.13u ng=1 m=1 mm_ok=1
Xxr2bkb1p x_r2b_kb x_r2b_b vdg vdg sg13_lv_pmos w=0.6u l=0.13u ng=1 m=1 mm_ok=1
Xxr2bkb1n x_r2b_kb x_r2b_b 0 0 sg13_lv_nmos w=0.3u l=0.13u ng=1 m=1 mm_ok=1
Xxr2bkb2p x_r2b_b x_r2b_kb vdg vdg sg13_lv_pmos w=0.6u l=0.13u ng=1 m=1 mm_ok=1
Xxr2bkb2n x_r2b_b x_r2b_kb 0 0 sg13_lv_nmos w=0.3u l=0.13u ng=1 m=1 mm_ok=1
Xxr3akq1p x_r3a_kq x_r3 vdg vdg sg13_lv_pmos w=0.6u l=0.13u ng=1 m=1 mm_ok=1
Xxr3akq1n x_r3a_kq x_r3 0 0 sg13_lv_nmos w=0.3u l=0.13u ng=1 m=1 mm_ok=1
Xxr3akq2p x_r3 x_r3a_kq vdg vdg sg13_lv_pmos w=0.6u l=0.13u ng=1 m=1 mm_ok=1
Xxr3akq2n x_r3 x_r3a_kq 0 0 sg13_lv_nmos w=0.3u l=0.13u ng=1 m=1 mm_ok=1
Xxr3aka1p x_r3a_ka x_r3a_a vdg vdg sg13_lv_pmos w=0.6u l=0.13u ng=1 m=1 mm_ok=1
Xxr3aka1n x_r3a_ka x_r3a_a 0 0 sg13_lv_nmos w=0.3u l=0.13u ng=1 m=1 mm_ok=1
Xxr3aka2p x_r3a_a x_r3a_ka vdg vdg sg13_lv_pmos w=0.6u l=0.13u ng=1 m=1 mm_ok=1
Xxr3aka2n x_r3a_a x_r3a_ka 0 0 sg13_lv_nmos w=0.3u l=0.13u ng=1 m=1 mm_ok=1
Xxr3akb1p x_r3a_kb x_r3a_b vdg vdg sg13_lv_pmos w=0.6u l=0.13u ng=1 m=1 mm_ok=1
Xxr3akb1n x_r3a_kb x_r3a_b 0 0 sg13_lv_nmos w=0.3u l=0.13u ng=1 m=1 mm_ok=1
Xxr3akb2p x_r3a_b x_r3a_kb vdg vdg sg13_lv_pmos w=0.6u l=0.13u ng=1 m=1 mm_ok=1
Xxr3akb2n x_r3a_b x_r3a_kb 0 0 sg13_lv_nmos w=0.3u l=0.13u ng=1 m=1 mm_ok=1
Xxr3bkq1p x_r3b_kq x_r3b vdg vdg sg13_lv_pmos w=0.6u l=0.13u ng=1 m=1 mm_ok=1
Xxr3bkq1n x_r3b_kq x_r3b 0 0 sg13_lv_nmos w=0.3u l=0.13u ng=1 m=1 mm_ok=1
Xxr3bkq2p x_r3b x_r3b_kq vdg vdg sg13_lv_pmos w=0.6u l=0.13u ng=1 m=1 mm_ok=1
Xxr3bkq2n x_r3b x_r3b_kq 0 0 sg13_lv_nmos w=0.3u l=0.13u ng=1 m=1 mm_ok=1
Xxr3bka1p x_r3b_ka x_r3b_a vdg vdg sg13_lv_pmos w=0.6u l=0.13u ng=1 m=1 mm_ok=1
Xxr3bka1n x_r3b_ka x_r3b_a 0 0 sg13_lv_nmos w=0.3u l=0.13u ng=1 m=1 mm_ok=1
Xxr3bka2p x_r3b_a x_r3b_ka vdg vdg sg13_lv_pmos w=0.6u l=0.13u ng=1 m=1 mm_ok=1
Xxr3bka2n x_r3b_a x_r3b_ka 0 0 sg13_lv_nmos w=0.3u l=0.13u ng=1 m=1 mm_ok=1
Xxr3bkb1p x_r3b_kb x_r3b_b vdg vdg sg13_lv_pmos w=0.6u l=0.13u ng=1 m=1 mm_ok=1
Xxr3bkb1n x_r3b_kb x_r3b_b 0 0 sg13_lv_nmos w=0.3u l=0.13u ng=1 m=1 mm_ok=1
Xxr3bkb2p x_r3b_b x_r3b_kb vdg vdg sg13_lv_pmos w=0.6u l=0.13u ng=1 m=1 mm_ok=1
Xxr3bkb2n x_r3b_b x_r3b_kb 0 0 sg13_lv_nmos w=0.3u l=0.13u ng=1 m=1 mm_ok=1
Xxr4akq1p x_r4a_kq x_r4 vdg vdg sg13_lv_pmos w=0.6u l=0.13u ng=1 m=1 mm_ok=1
Xxr4akq1n x_r4a_kq x_r4 0 0 sg13_lv_nmos w=0.3u l=0.13u ng=1 m=1 mm_ok=1
Xxr4akq2p x_r4 x_r4a_kq vdg vdg sg13_lv_pmos w=0.6u l=0.13u ng=1 m=1 mm_ok=1
Xxr4akq2n x_r4 x_r4a_kq 0 0 sg13_lv_nmos w=0.3u l=0.13u ng=1 m=1 mm_ok=1
Xxr4aka1p x_r4a_ka x_r4a_a vdg vdg sg13_lv_pmos w=0.6u l=0.13u ng=1 m=1 mm_ok=1
Xxr4aka1n x_r4a_ka x_r4a_a 0 0 sg13_lv_nmos w=0.3u l=0.13u ng=1 m=1 mm_ok=1
Xxr4aka2p x_r4a_a x_r4a_ka vdg vdg sg13_lv_pmos w=0.6u l=0.13u ng=1 m=1 mm_ok=1
Xxr4aka2n x_r4a_a x_r4a_ka 0 0 sg13_lv_nmos w=0.3u l=0.13u ng=1 m=1 mm_ok=1
Xxr4akb1p x_r4a_kb x_r4a_b vdg vdg sg13_lv_pmos w=0.6u l=0.13u ng=1 m=1 mm_ok=1
Xxr4akb1n x_r4a_kb x_r4a_b 0 0 sg13_lv_nmos w=0.3u l=0.13u ng=1 m=1 mm_ok=1
Xxr4akb2p x_r4a_b x_r4a_kb vdg vdg sg13_lv_pmos w=0.6u l=0.13u ng=1 m=1 mm_ok=1
Xxr4akb2n x_r4a_b x_r4a_kb 0 0 sg13_lv_nmos w=0.3u l=0.13u ng=1 m=1 mm_ok=1
Xxr4bkq1p x_r4b_kq x_r4b vdg vdg sg13_lv_pmos w=0.6u l=0.13u ng=1 m=1 mm_ok=1
Xxr4bkq1n x_r4b_kq x_r4b 0 0 sg13_lv_nmos w=0.3u l=0.13u ng=1 m=1 mm_ok=1
Xxr4bkq2p x_r4b x_r4b_kq vdg vdg sg13_lv_pmos w=0.6u l=0.13u ng=1 m=1 mm_ok=1
Xxr4bkq2n x_r4b x_r4b_kq 0 0 sg13_lv_nmos w=0.3u l=0.13u ng=1 m=1 mm_ok=1
Xxr4bka1p x_r4b_ka x_r4b_a vdg vdg sg13_lv_pmos w=0.6u l=0.13u ng=1 m=1 mm_ok=1
Xxr4bka1n x_r4b_ka x_r4b_a 0 0 sg13_lv_nmos w=0.3u l=0.13u ng=1 m=1 mm_ok=1
Xxr4bka2p x_r4b_a x_r4b_ka vdg vdg sg13_lv_pmos w=0.6u l=0.13u ng=1 m=1 mm_ok=1
Xxr4bka2n x_r4b_a x_r4b_ka 0 0 sg13_lv_nmos w=0.3u l=0.13u ng=1 m=1 mm_ok=1
Xxr4bkb1p x_r4b_kb x_r4b_b vdg vdg sg13_lv_pmos w=0.6u l=0.13u ng=1 m=1 mm_ok=1
Xxr4bkb1n x_r4b_kb x_r4b_b 0 0 sg13_lv_nmos w=0.3u l=0.13u ng=1 m=1 mm_ok=1
Xxr4bkb2p x_r4b_b x_r4b_kb vdg vdg sg13_lv_pmos w=0.6u l=0.13u ng=1 m=1 mm_ok=1
Xxr4bkb2n x_r4b_b x_r4b_kb 0 0 sg13_lv_nmos w=0.3u l=0.13u ng=1 m=1 mm_ok=1
**.ends
.end
